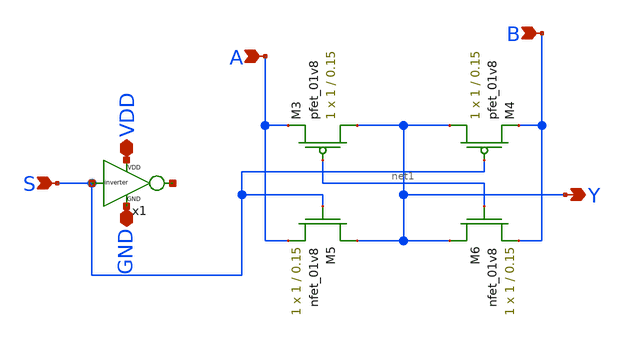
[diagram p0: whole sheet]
** sch_path: Final DAC files/schematics/Mux/2_1_mux.sch
**.subckt 2_1_mux Y S A B GND VDD
*.opin Y
*.ipin S
*.ipin A
*.ipin B
*.iopin GND
*.iopin VDD
XM3 Y net1 A VDD sky130_fd_pr__pfet_01v8 L=0.15 W=1 nf=1 ad='int((nf+1)/2) * W/nf * 0.29' as='int((nf+2)/2) * W/nf * 0.29'
+ pd='2*int((nf+1)/2) * (W/nf + 0.29)' ps='2*int((nf+2)/2) * (W/nf + 0.29)' nrd='0.29 / W' nrs='0.29 / W'
+ sa=0 sb=0 sd=0 mult=1 m=1
XM4 Y S B VDD sky130_fd_pr__pfet_01v8 L=0.15 W=1 nf=1 ad='int((nf+1)/2) * W/nf * 0.29' as='int((nf+2)/2) * W/nf * 0.29'
+ pd='2*int((nf+1)/2) * (W/nf + 0.29)' ps='2*int((nf+2)/2) * (W/nf + 0.29)' nrd='0.29 / W' nrs='0.29 / W'
+ sa=0 sb=0 sd=0 mult=1 m=1
XM5 Y S A GND sky130_fd_pr__nfet_01v8 L=0.15 W=1 nf=1 ad='int((nf+1)/2) * W/nf * 0.29' as='int((nf+2)/2) * W/nf * 0.29'
+ pd='2*int((nf+1)/2) * (W/nf + 0.29)' ps='2*int((nf+2)/2) * (W/nf + 0.29)' nrd='0.29 / W' nrs='0.29 / W'
+ sa=0 sb=0 sd=0 mult=1 m=1
XM6 Y net1 B GND sky130_fd_pr__nfet_01v8 L=0.15 W=1 nf=1 ad='int((nf+1)/2) * W/nf * 0.29' as='int((nf+2)/2) * W/nf * 0.29'
+ pd='2*int((nf+1)/2) * (W/nf + 0.29)' ps='2*int((nf+2)/2) * (W/nf + 0.29)' nrd='0.29 / W' nrs='0.29 / W'
+ sa=0 sb=0 sd=0 mult=1 m=1
x1 VDD S net2 GND inverter
**.ends

* expanding   symbol:  /home/madvlsi/dev/git/7-bit-D-A-converter-MP4-MADVLSI/Final DAC
*+ files/schematics/Inverter/inverter.sym # of pins=4
** sym_path: schematics/ieee DAC/inverter.sym
** sch_path: schematics/ieee DAC/inverter.sch
.subckt inverter VDD A Y GND
*.ipin A
*.iopin VDD
*.iopin GND
*.opin Y
XM1 Y A GND GND sky130_fd_pr__nfet_01v8 L=0.5 W=12 nf=1 ad='int((nf+1)/2) * W/nf * 0.29' as='int((nf+2)/2) * W/nf * 0.29'
+ pd='2*int((nf+1)/2) * (W/nf + 0.29)' ps='2*int((nf+2)/2) * (W/nf + 0.29)' nrd='0.29 / W' nrs='0.29 / W'
+ sa=0 sb=0 sd=0 mult=1 m=1
XM2 Y A VDD VDD sky130_fd_pr__pfet_01v8 L=0.5 W=12 nf=1 ad='int((nf+1)/2) * W/nf * 0.29' as='int((nf+2)/2) * W/nf * 0.29'
+ pd='2*int((nf+1)/2) * (W/nf + 0.29)' ps='2*int((nf+2)/2) * (W/nf + 0.29)' nrd='0.29 / W' nrs='0.29 / W'
+ sa=0 sb=0 sd=0 mult=1 m=1
.ends

.end
